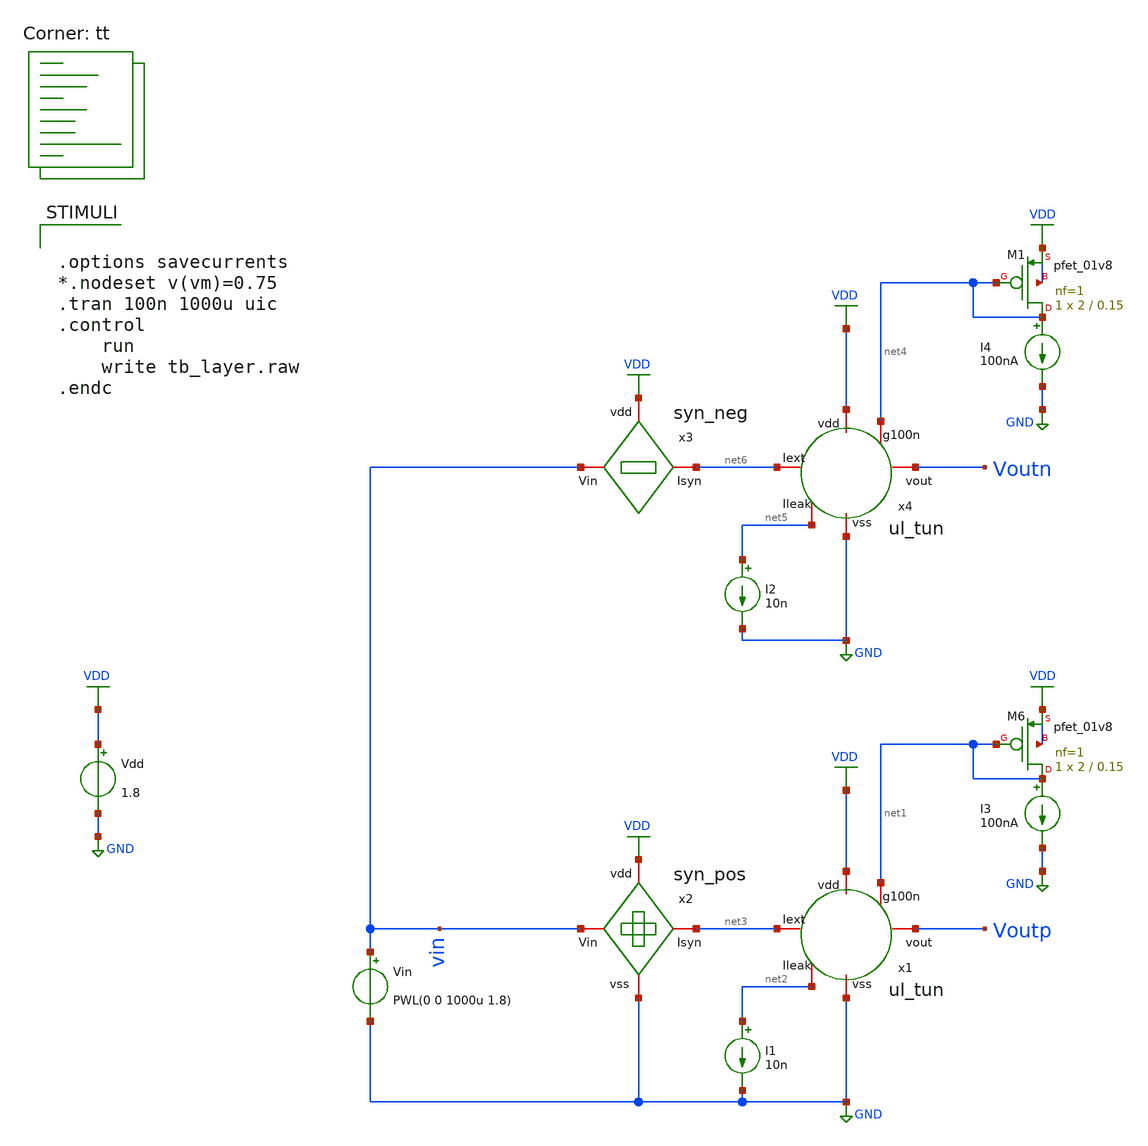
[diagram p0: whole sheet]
** sch_path: Neuron/ultralif/tb_layer.sch
**.subckt tb_layer
I1 net2 GND 10n
Vdd VDD GND 1.8
I3 net1 GND 100nA
Vin vin GND PWL(0 0 1000u 1.8)
XM6 net1 net1 VDD VDD sky130_fd_pr__pfet_01v8 L=0.15 W=2 nf=1 ad='int((nf+1)/2) * W/nf * 0.29' as='int((nf+2)/2) * W/nf * 0.29'
+ pd='2*int((nf+1)/2) * (W/nf + 0.29)' ps='2*int((nf+2)/2) * (W/nf + 0.29)' nrd='0.29 / W' nrs='0.29 / W'
+ sa=0 sb=0 sd=0 mult=1 m=1
x2 VDD vin net3 GND syn_pos
x1 net3 VDD net1 Voutp net2 GND ul_tun
I2 net5 GND 10n
I4 net4 GND 100nA
XM1 net4 net4 VDD VDD sky130_fd_pr__pfet_01v8 L=0.15 W=2 nf=1 ad='int((nf+1)/2) * W/nf * 0.29' as='int((nf+2)/2) * W/nf * 0.29'
+ pd='2*int((nf+1)/2) * (W/nf + 0.29)' ps='2*int((nf+2)/2) * (W/nf + 0.29)' nrd='0.29 / W' nrs='0.29 / W'
+ sa=0 sb=0 sd=0 mult=1 m=1
x3 VDD vin net6 syn_neg
x4 net6 VDD net4 Voutn net5 GND ul_tun
**** begin user architecture code
.lib $::SKYWATER_MODELS/sky130.lib.spice tt
**** end user architecture code
**.ends

* expanding   symbol:  syn_pos.sym # of pins=4
** sym_path: Neuron/ultralif/syn_pos.sym
** sch_path: Neuron/ultralif/syn_pos.sch
.subckt syn_pos vdd Vin Isyn vss
*.iopin Vin
*.iopin vdd
*.iopin vss
*.iopin Isyn
XM9 Isyn vx vdd vdd sky130_fd_pr__pfet_01v8 L=1 W=0.5 nf=1 ad='int((nf+1)/2) * W/nf * 0.29' as='int((nf+2)/2) * W/nf * 0.29'
+ pd='2*int((nf+1)/2) * (W/nf + 0.29)' ps='2*int((nf+2)/2) * (W/nf + 0.29)' nrd='0.29 / W' nrs='0.29 / W'
+ sa=0 sb=0 sd=0 mult=1 m=1
XM10 vx vx vdd vdd sky130_fd_pr__pfet_01v8 L=0.15 W=0.5 nf=1 ad='int((nf+1)/2) * W/nf * 0.29' as='int((nf+2)/2) * W/nf * 0.29'
+ pd='2*int((nf+1)/2) * (W/nf + 0.29)' ps='2*int((nf+2)/2) * (W/nf + 0.29)' nrd='0.29 / W' nrs='0.29 / W'
+ sa=0 sb=0 sd=0 mult=5 m=5
XM12 vx Vin vss vss sky130_fd_pr__nfet_01v8 L=1 W=0.4 nf=1 ad='int((1 + 1)/2) * 0.4 / 1 * 0.29' as='int((1 + 2)/2) * 0.4 / 1 * 0.29'
+ pd='2*int((1 + 1)/2) * (0.4 / 1 + 0.29)' ps='2*int((1 + 2)/2) * (0.4 / 1 + 0.29)' nrd='0.29 / 0.4 ' nrs='0.29 / 0.4 '
+ sa=0 sb=0 sd=0 mult=1 m=1
.ends


* expanding   symbol:  ul_tun.sym # of pins=6
** sym_path: Neuron/ultralif/ul_tun.sym
** sch_path: Neuron/ultralif/ul_tun.sch
.subckt ul_tun Iext vdd g100n vout Ileak vss
*.iopin Iext
*.iopin vout
*.iopin vss
*.iopin Ileak
*.iopin vdd
*.iopin g100n
XM1 Ileak Ileak net1 vdd sky130_fd_pr__pfet_01v8 L=10 W=1 nf=1 ad='int((nf+1)/2) * W/nf * 0.29' as='int((nf+2)/2) * W/nf * 0.29'
+ pd='2*int((nf+1)/2) * (W/nf + 0.29)' ps='2*int((nf+2)/2) * (W/nf + 0.29)' nrd='0.29 / W' nrs='0.29 / W'
+ sa=0 sb=0 sd=0 mult=1 m=1
XM2 Ileak net2 net1 vdd sky130_fd_pr__pfet_01v8 L=0.15 W=1.5 nf=1 ad='int((nf+1)/2) * W/nf * 0.29' as='int((nf+2)/2) * W/nf * 0.29'
+ pd='2*int((nf+1)/2) * (W/nf + 0.29)' ps='2*int((nf+2)/2) * (W/nf + 0.29)' nrd='0.29 / W' nrs='0.29 / W'
+ sa=0 sb=0 sd=0 mult=1 m=1
XM3 net2 net2 net1 vdd sky130_fd_pr__pfet_01v8 L=0.15 W=15 nf=1 ad='int((nf+1)/2) * W/nf * 0.29' as='int((nf+2)/2) * W/nf * 0.29'
+ pd='2*int((nf+1)/2) * (W/nf + 0.29)' ps='2*int((nf+2)/2) * (W/nf + 0.29)' nrd='0.29 / W' nrs='0.29 / W'
+ sa=0 sb=0 sd=0 mult=1 m=1
XM4 net2 Ileak vss vss sky130_fd_pr__nfet_01v8 L=4 W=1 nf=1 ad='int((1 + 1)/2) * 1 / 1 * 0.29' as='int((1 + 2)/2) * 1 / 1 * 0.29'
+ pd='2*int((1 + 1)/2) * (1 / 1 + 0.29)' ps='2*int((1 + 2)/2) * (1 / 1 + 0.29)' nrd='0.29 / 1 ' nrs='0.29 / 1 '
+ sa=0 sb=0 sd=0 mult=1 m=1
C1 net1 vss 1p m=1
XM5 vout_n Ileak vss vss sky130_fd_pr__nfet_01v8 L=0.15 W=1 nf=1 ad='int((1 + 1)/2) * 1 / 1 * 0.29' as='int((1 + 2)/2) * 1 / 1 * 0.29'
+ pd='2*int((1 + 1)/2) * (1 / 1 + 0.29)' ps='2*int((1 + 2)/2) * (1 / 1 + 0.29)' nrd='0.29 / 1 ' nrs='0.29 / 1 '
+ sa=0 sb=0 sd=0 mult=1 m=1
XM6 vout_n g100n vdd vdd sky130_fd_pr__pfet_01v8 L=0.15 W=2 nf=1 ad='int((nf+1)/2) * W/nf * 0.29' as='int((nf+2)/2) * W/nf * 0.29'
+ pd='2*int((nf+1)/2) * (W/nf + 0.29)' ps='2*int((nf+2)/2) * (W/nf + 0.29)' nrd='0.29 / W' nrs='0.29 / W'
+ sa=0 sb=0 sd=0 mult=1 m=1
XM7 vout vout_n vss vss sky130_fd_pr__nfet_01v8 L=0.15 W=1 nf=1 ad='int((1 + 1)/2) * 1 / 1 * 0.29' as='int((1 + 2)/2) * 1 / 1 * 0.29'
+ pd='2*int((1 + 1)/2) * (1 / 1 + 0.29)' ps='2*int((1 + 2)/2) * (1 / 1 + 0.29)' nrd='0.29 / 1 ' nrs='0.29 / 1 '
+ sa=0 sb=0 sd=0 mult=1 m=1
XM8 vout vout_n vdd vdd sky130_fd_pr__pfet_01v8 L=0.15 W=2 nf=1 ad='int((nf+1)/2) * W/nf * 0.29' as='int((nf+2)/2) * W/nf * 0.29'
+ pd='2*int((nf+1)/2) * (W/nf + 0.29)' ps='2*int((nf+2)/2) * (W/nf + 0.29)' nrd='0.29 / W' nrs='0.29 / W'
+ sa=0 sb=0 sd=0 mult=1 m=1
vext Iext net1 0
**** begin user architecture code


.save i(vext)


**** end user architecture code
.ends


* expanding   symbol:  syn_neg.sym # of pins=3
** sym_path: Neuron/ultralif/syn_neg.sym
** sch_path: Neuron/ultralif/syn_neg.sch
.subckt syn_neg vdd Vin Isyn
*.iopin Vin
*.iopin Isyn
*.iopin vdd
XM10 Isyn Vin vx vdd sky130_fd_pr__pfet_01v8 L=30 W=0.5 nf=1 ad='int((nf+1)/2) * W/nf * 0.29' as='int((nf+2)/2) * W/nf * 0.29'
+ pd='2*int((nf+1)/2) * (W/nf + 0.29)' ps='2*int((nf+2)/2) * (W/nf + 0.29)' nrd='0.29 / W' nrs='0.29 / W'
+ sa=0 sb=0 sd=0 mult=1 m=1
XM1 vx Vin vdd vdd sky130_fd_pr__pfet_01v8 L=30 W=0.5 nf=1 ad='int((nf+1)/2) * W/nf * 0.29' as='int((nf+2)/2) * W/nf * 0.29'
+ pd='2*int((nf+1)/2) * (W/nf + 0.29)' ps='2*int((nf+2)/2) * (W/nf + 0.29)' nrd='0.29 / W' nrs='0.29 / W'
+ sa=0 sb=0 sd=0 mult=1 m=1
.ends

.GLOBAL GND
.GLOBAL VDD
**** begin user architecture code


.options savecurrents
*.nodeset v(vm)=0.75
.tran 100n 1000u uic
.control
	run
	write tb_layer.raw
.endc


**** end user architecture code
.end
